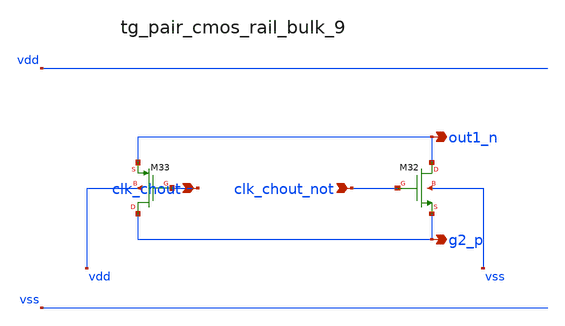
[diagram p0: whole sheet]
** sch_path: analog-db/raw/ia_003_fan_chopper_pf/hier/blocks/tg_pair_cmos_rail_bulk_9.sch
**.subckt tg_pair_cmos_rail_bulk_9 clk_chout clk_chout_not out1_n g2_p
*.ipin clk_chout
*.ipin clk_chout_not
*.opin out1_n
*.opin g2_p
XM32 out1_n clk_chout_not g2_p vss sg13_lv_nmos w=x_dut_xm32_w l=x_dut_xm32_l ng=1 m=x_dut_xm32_m
XM33 g2_p clk_chout out1_n vdd sg13_lv_pmos w=x_dut_xm33_w l=x_dut_xm33_l ng=1 m=x_dut_xm33_m
**.ends
.end
